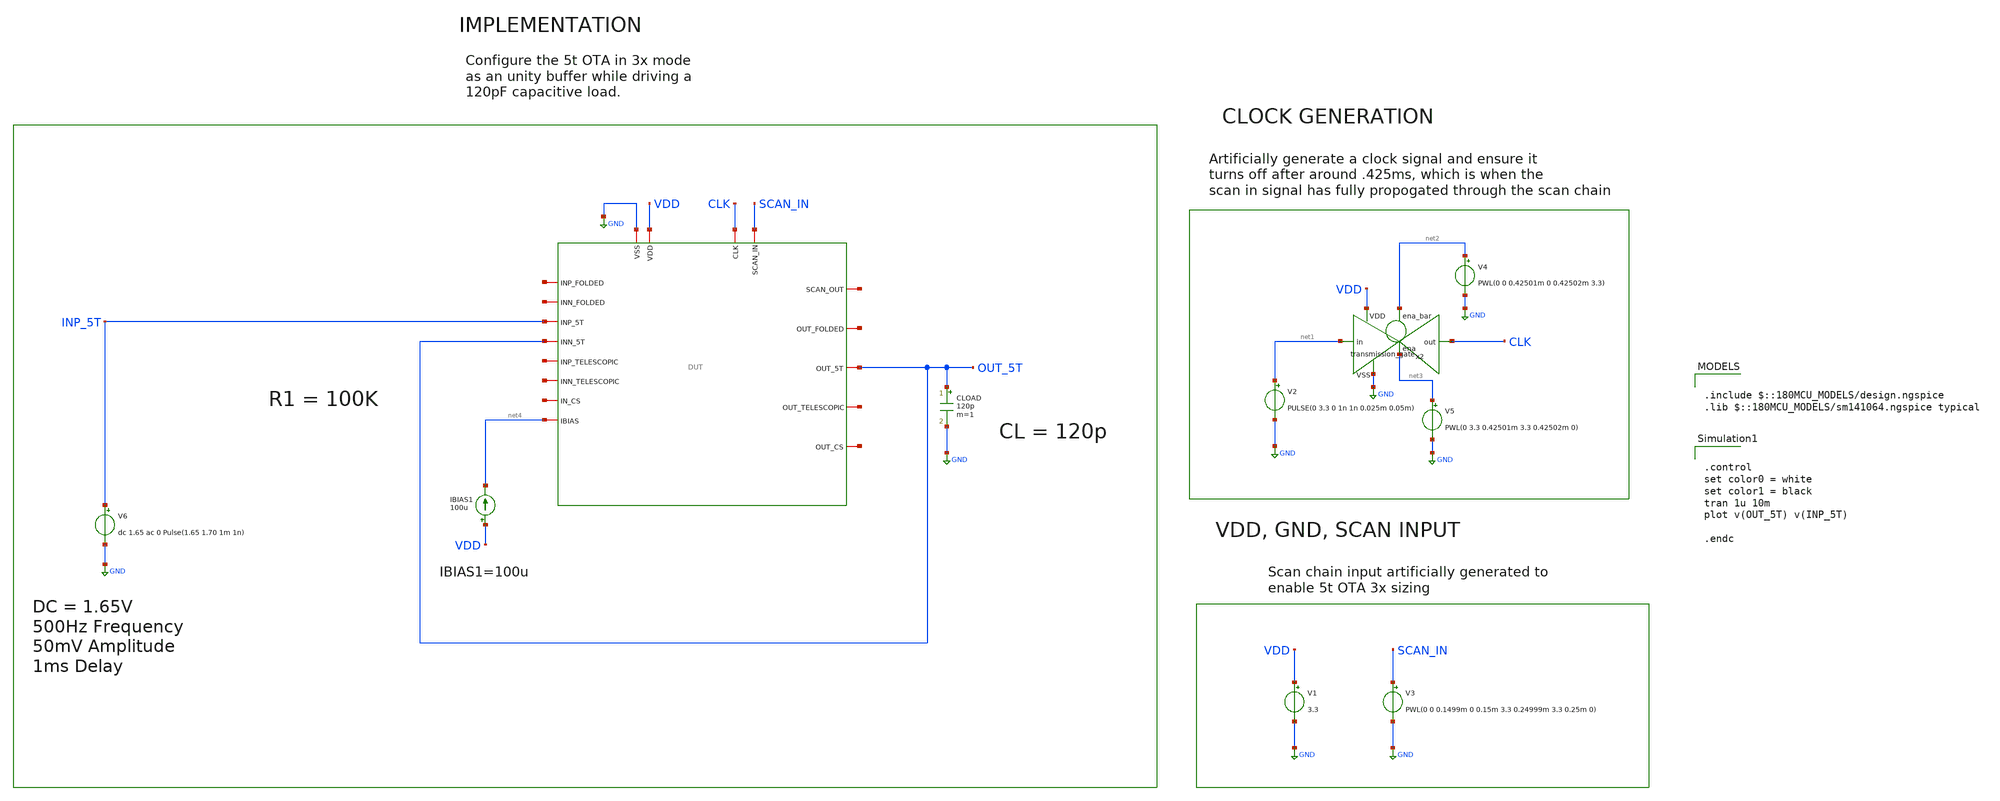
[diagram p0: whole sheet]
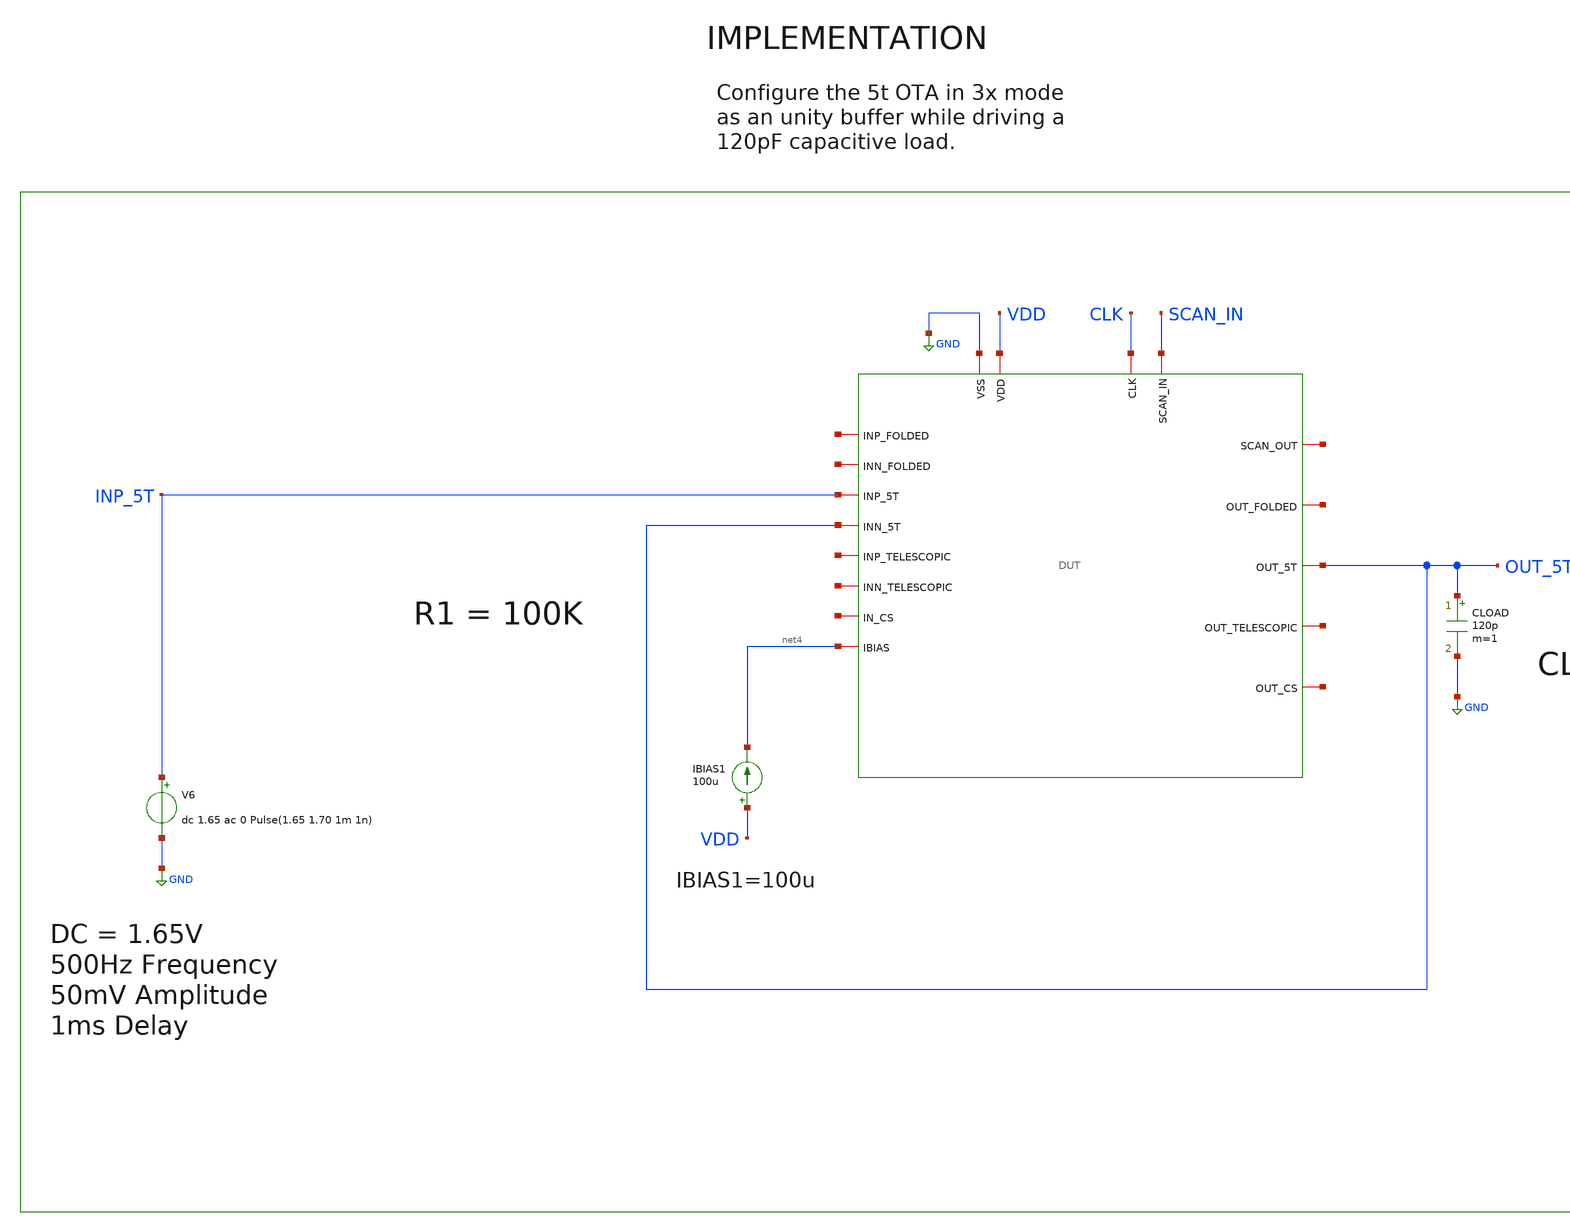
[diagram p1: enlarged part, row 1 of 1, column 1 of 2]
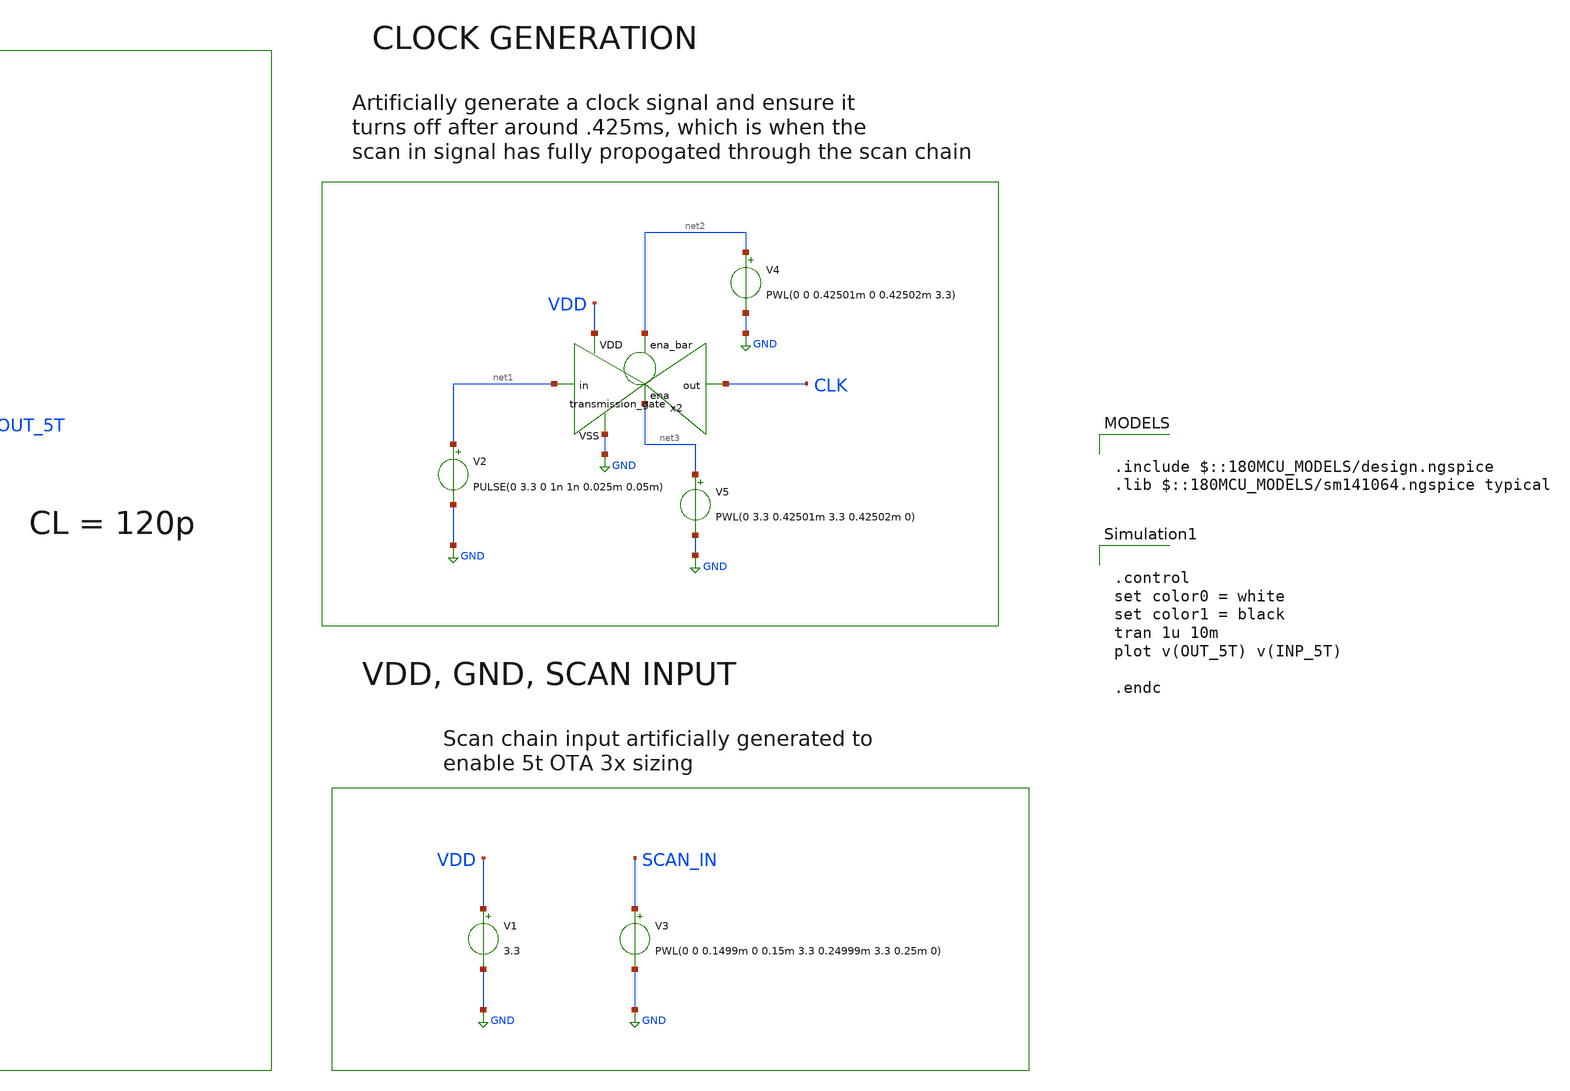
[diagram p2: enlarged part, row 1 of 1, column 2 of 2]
** sch_path: designs/libs/core_tb/sl/ota_5t/5t_unity_step_3x.sch
**.subckt 5t_unity_step_3x
V3 SCAN_IN GND PWL(0 0 0.1499m 0 0.15m 3.3 0.24999m 3.3 0.25m 0)
V1 VDD GND 3.3
V2 net1 GND PULSE(0 3.3 0 1n 1n 0.025m 0.05m)
x2 net2 VDD CLK net1 GND net3 transmission_gate
V4 net2 GND PWL(0 0 0.42501m 0 0.42502m 3.3)
V5 net3 GND PWL(0 3.3 0.42501m 3.3 0.42502m 0)
IBIAS1 VDD net4 100u
CLOAD OUT_5T GND 120p m=1
V6 INP_5T GND dc 1.65 ac 0 Pulse(1.65 1.70 1m 1n)
x1 CLK net5 SCAN_IN GND VDD net6 net7 OUT_5T net4 net8 INP_5T OUT_5T net9 net10 net11 net12 net13
+ DUT
**** begin user architecture code

.include $::180MCU_MODELS/design.ngspice
.lib $::180MCU_MODELS/sm141064.ngspice typical



.control
set color0 = white
set color1 = black
tran 1u 10m
plot v(OUT_5T) v(INP_5T)

.endc


**** end user architecture code
**.ends
.GLOBAL GND
.end
